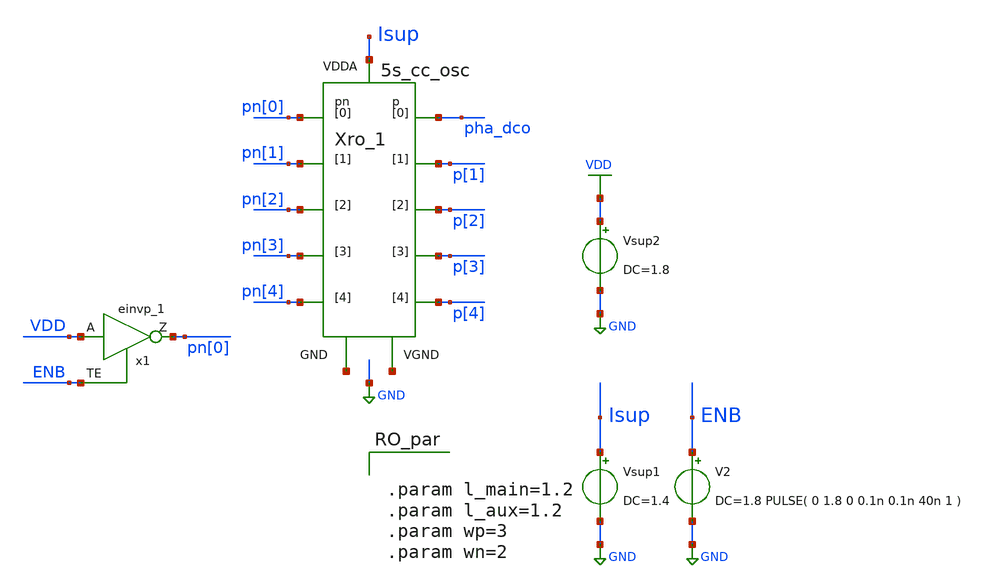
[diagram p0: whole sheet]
** sch_path: xschem/tb/DCO_design.sch

.include $::SKYWATER_STDCELLS/sky130_fd_sc_hd.spice
.lib $::SKYWATER_MODELS/sky130.lib.spice tt

**.subckt DCO_design
x1 VDD ENB GND GND VDD VDD pn[0] sky130_fd_sc_hd__einvp_1
V2 ENB GND DC=1.8 PULSE( 0 1.8 0 0.1n 0.1n 40n 1 )
Vsup1 Isup GND DC=1.4
Vsup2 VDD GND DC=1.8
Xro_1 net1 Isup pha_dco p[1] p[2] p[3] p[4] pn[0] pn[1] pn[2] pn[3] pn[4] net2 5s_cc_osc
**.ends
.GLOBAL GND
.GLOBAL VDD
**** begin user architecture code


.control
set nobreak
set num_threads=8
set test_mode = 1
* mode = 0: operation testing    1:  frequency extraction    2:  power consumption
if ($test_mode = 0)
    TRAN 1n 16u
    plot pha_dco
    MEAS TRAN prd TRIG pha_dco VAL=0.8 RISE=20 TARG pha_dco VAL=0.8 RISE=30
    let freq = 10/prd
    echo "frequency: "
    print freq
end
if ($test_mode = 1)
    let Vlow = 1
    let Vlimit = 1.81     $ set upper bound for sweeping
    let Vsweep = 0.1      $ set step size for sweeping
    let NoPoints=(Vlimit-Vlow)/Vsweep+2    $ set number of points for sweeping
    let freq =unitvec(NoPoints)
    let Vin  =unitvec(NoPoints)
    let Vin[0]=Vlow
    let ix=0
    while Vin[ix] < Vlimit
        alter Vsup1 DC=Vin[ix]
        TRAN 1n 16u
        MEAS TRAN prd TRIG pha_dco VAL=0.8 RISE=30 TARG pha_dco VAL=0.8 RISE =40
        let freq[ix] = 10/prd
        let ix = ix+1
        Let Vin[ix] = Vin[ix-1]+Vsweep
    end
   print Vin freq
end
if ($test_mode = 2)
    save vdd @Vsup1[i] pha_dco
    TRAN 0.1n 5u
    MEAS TRAN I_vco AVG @Vsup1[i] FROM=3u TO=4u
    MEAS TRAN V_vco AVG vdd FROM=3u TO=4u
    let Power=I_vco*V_vco
    print Power
end
.endc




.param l_main=1.2
.param l_aux=1.2
.param wp=3
.param wn=2

**** end user architecture code
.end
